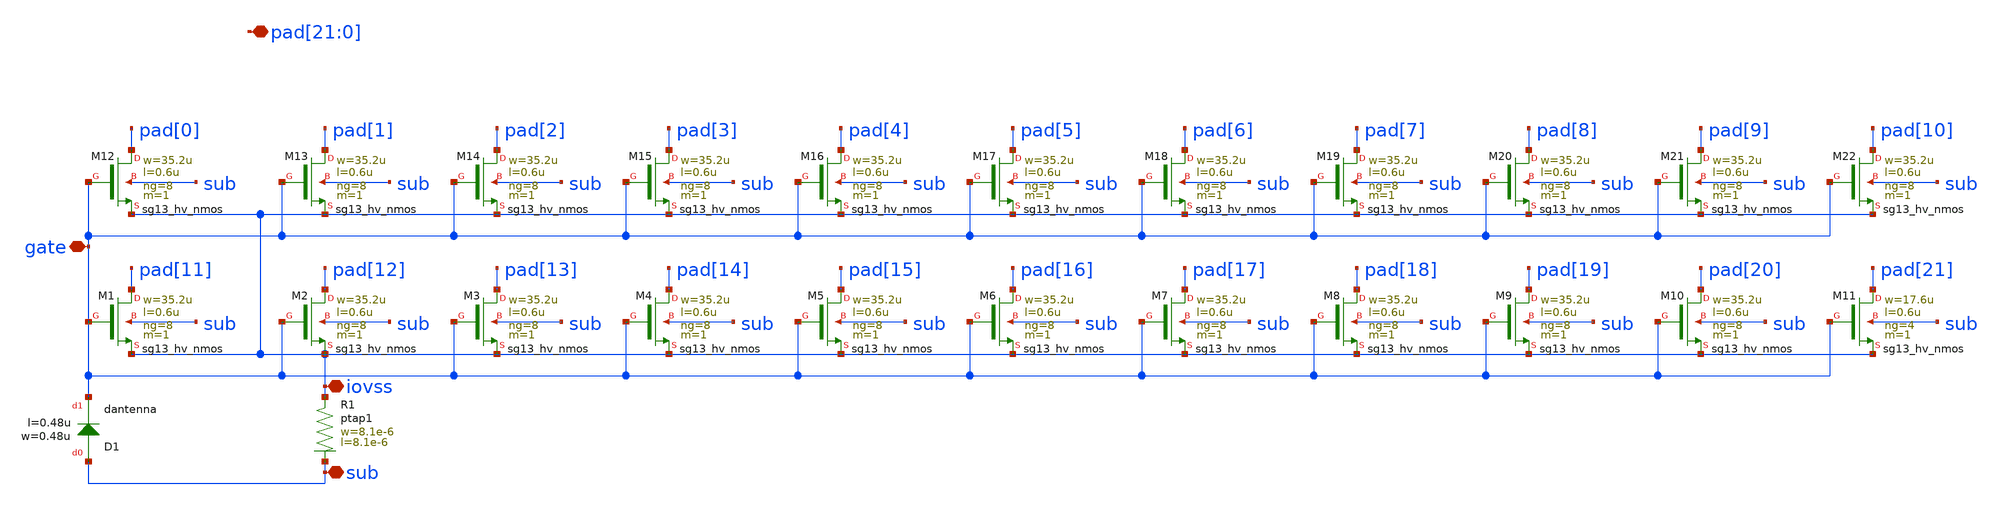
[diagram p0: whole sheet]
** sch_path: MSPHY6034-main/schematic/xschem/openpdk-libraries/ihp-sg13g2/sg13g2_io/xschem/sg13g2_Clamp_N43N43D4R.sch
**.subckt sg13g2_Clamp_N43N43D4R iovss
*+ pad[21],pad[20],pad[19],pad[18],pad[17],pad[16],pad[15],pad[14],pad[13],pad[12],pad[11],pad[10],pad[9],pad[8],pad[7],pad[6],pad[5],pad[4],pad[3],pad[2],pad[1],pad[0] sub gate
*.iopin iovss
*.iopin
*+ pad[21],pad[20],pad[19],pad[18],pad[17],pad[16],pad[15],pad[14],pad[13],pad[12],pad[11],pad[10],pad[9],pad[8],pad[7],pad[6],pad[5],pad[4],pad[3],pad[2],pad[1],pad[0]
*.iopin sub
*.iopin gate
XR1 iovss sub ptap1 R=9.999 w=8.1e-6 l=8.1e-6
XM1 pad[11] gate iovss sub sg13_hv_nmos w=35.2u l=0.6u ng=8 m=1 mm_ok=1
XM2 pad[12] gate iovss sub sg13_hv_nmos w=35.2u l=0.6u ng=8 m=1 mm_ok=1
XM3 pad[13] gate iovss sub sg13_hv_nmos w=35.2u l=0.6u ng=8 m=1 mm_ok=1
XM4 pad[14] gate iovss sub sg13_hv_nmos w=35.2u l=0.6u ng=8 m=1 mm_ok=1
XM5 pad[15] gate iovss sub sg13_hv_nmos w=35.2u l=0.6u ng=8 m=1 mm_ok=1
XM6 pad[16] gate iovss sub sg13_hv_nmos w=35.2u l=0.6u ng=8 m=1 mm_ok=1
XM7 pad[17] gate iovss sub sg13_hv_nmos w=35.2u l=0.6u ng=8 m=1 mm_ok=1
XM8 pad[18] gate iovss sub sg13_hv_nmos w=35.2u l=0.6u ng=8 m=1 mm_ok=1
XM9 pad[19] gate iovss sub sg13_hv_nmos w=35.2u l=0.6u ng=8 m=1 mm_ok=1
XM10 pad[20] gate iovss sub sg13_hv_nmos w=35.2u l=0.6u ng=8 m=1 mm_ok=1
XM11 pad[21] gate iovss sub sg13_hv_nmos w=17.6u l=0.6u ng=4 m=1 mm_ok=1
XD1 sub gate dantenna l=0.48u w=0.48u
XM12 pad[0] gate iovss sub sg13_hv_nmos w=35.2u l=0.6u ng=8 m=1 mm_ok=1
XM13 pad[1] gate iovss sub sg13_hv_nmos w=35.2u l=0.6u ng=8 m=1 mm_ok=1
XM14 pad[2] gate iovss sub sg13_hv_nmos w=35.2u l=0.6u ng=8 m=1 mm_ok=1
XM15 pad[3] gate iovss sub sg13_hv_nmos w=35.2u l=0.6u ng=8 m=1 mm_ok=1
XM16 pad[4] gate iovss sub sg13_hv_nmos w=35.2u l=0.6u ng=8 m=1 mm_ok=1
XM17 pad[5] gate iovss sub sg13_hv_nmos w=35.2u l=0.6u ng=8 m=1 mm_ok=1
XM18 pad[6] gate iovss sub sg13_hv_nmos w=35.2u l=0.6u ng=8 m=1 mm_ok=1
XM19 pad[7] gate iovss sub sg13_hv_nmos w=35.2u l=0.6u ng=8 m=1 mm_ok=1
XM20 pad[8] gate iovss sub sg13_hv_nmos w=35.2u l=0.6u ng=8 m=1 mm_ok=1
XM21 pad[9] gate iovss sub sg13_hv_nmos w=35.2u l=0.6u ng=8 m=1 mm_ok=1
XM22 pad[10] gate iovss sub sg13_hv_nmos w=35.2u l=0.6u ng=8 m=1 mm_ok=1
**.ends
.end
